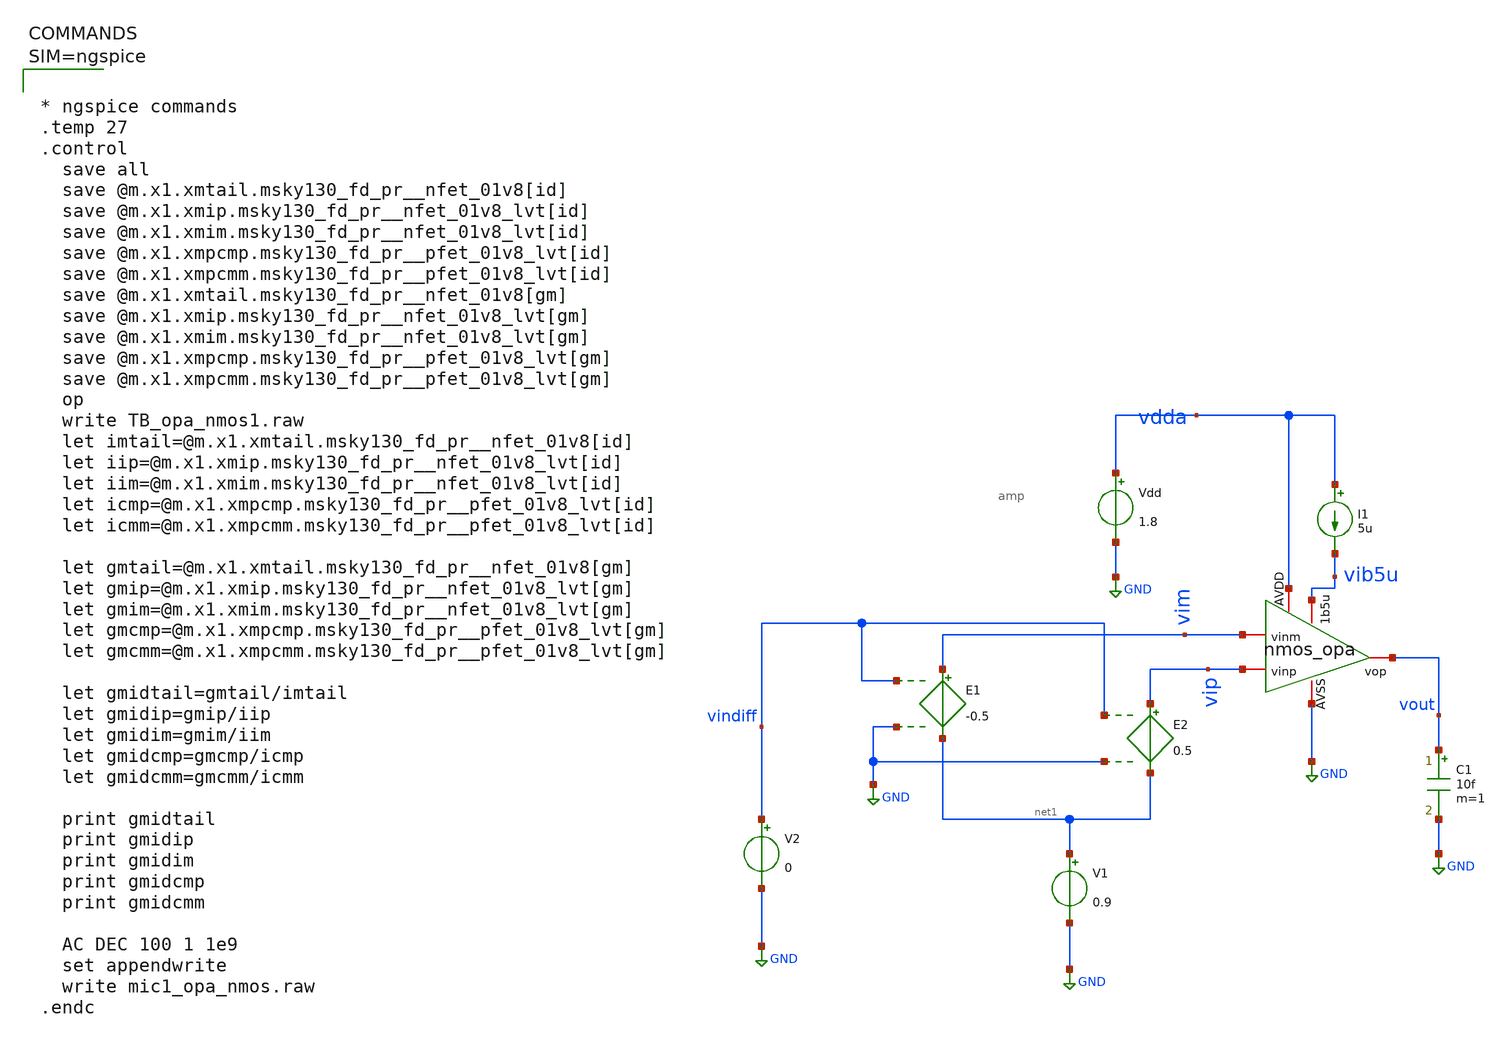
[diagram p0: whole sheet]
** sch_path: work/xschem/mic1_opa_nmos.sch
**.subckt mic1_opa_nmos
E1 vim net1 vindiff GND -0.5
E2 vip net1 vindiff GND 0.5
V1 net1 GND 0.9
V2 vindiff GND 0
Vdd vdda GND 1.8
I1 vdda vib5u 5u
C1 vout GND 10f m=1
x1 vdda vout vim vip vib5u GND amp
**** begin user architecture code

** opencircuitdesign pdks install
.lib $::SKYWATER_MODELS/sky130.lib.spice tt




* ngspice commands
.temp 27
.control
  save all
  save @m.x1.xmtail.msky130_fd_pr__nfet_01v8[id]
  save @m.x1.xmip.msky130_fd_pr__nfet_01v8_lvt[id]
  save @m.x1.xmim.msky130_fd_pr__nfet_01v8_lvt[id]
  save @m.x1.xmpcmp.msky130_fd_pr__pfet_01v8_lvt[id]
  save @m.x1.xmpcmm.msky130_fd_pr__pfet_01v8_lvt[id]
  save @m.x1.xmtail.msky130_fd_pr__nfet_01v8[gm]
  save @m.x1.xmip.msky130_fd_pr__nfet_01v8_lvt[gm]
  save @m.x1.xmim.msky130_fd_pr__nfet_01v8_lvt[gm]
  save @m.x1.xmpcmp.msky130_fd_pr__pfet_01v8_lvt[gm]
  save @m.x1.xmpcmm.msky130_fd_pr__pfet_01v8_lvt[gm]
  op
  write TB_opa_nmos1.raw
  let imtail=@m.x1.xmtail.msky130_fd_pr__nfet_01v8[id]
  let iip=@m.x1.xmip.msky130_fd_pr__nfet_01v8_lvt[id]
  let iim=@m.x1.xmim.msky130_fd_pr__nfet_01v8_lvt[id]
  let icmp=@m.x1.xmpcmp.msky130_fd_pr__pfet_01v8_lvt[id]
  let icmm=@m.x1.xmpcmm.msky130_fd_pr__pfet_01v8_lvt[id]

  let gmtail=@m.x1.xmtail.msky130_fd_pr__nfet_01v8[gm]
  let gmip=@m.x1.xmip.msky130_fd_pr__nfet_01v8_lvt[gm]
  let gmim=@m.x1.xmim.msky130_fd_pr__nfet_01v8_lvt[gm]
  let gmcmp=@m.x1.xmpcmp.msky130_fd_pr__pfet_01v8_lvt[gm]
  let gmcmm=@m.x1.xmpcmm.msky130_fd_pr__pfet_01v8_lvt[gm]

  let gmidtail=gmtail/imtail
  let gmidip=gmip/iip
  let gmidim=gmim/iim
  let gmidcmp=gmcmp/icmp
  let gmidcmm=gmcmm/icmm

  print gmidtail
  print gmidip
  print gmidim
  print gmidcmp
  print gmidcmm

  AC DEC 100 1 1e9
  set appendwrite
  write mic1_opa_nmos.raw
.endc




**** end user architecture code
**.ends

* expanding   symbol:  amp.sym # of pins=6
** sym_path: work/xschem/amp.sym
** sch_path: work/xschem/amp.sch
.subckt amp AVDD vop vinm vinp 1b5u AVSS
*.iopin vop
*.iopin vinp
*.iopin vinm
*.iopin 1b5u
*.iopin AVSS
*.iopin AVDD
XMtail net1 1b5u AVSS AVSS sky130_fd_pr__nfet_01v8 L=1 W=5 nf=1 ad='int((1 + 1)/2) * 5 / 1 * 0.29' as='int((1 + 2)/2) * 5 / 1 * 0.29'
+ pd='2*int((1 + 1)/2) * (5 / 1 + 0.29)' ps='2*int((1 + 2)/2) * (5 / 1 + 0.29)' nrd='0.29 / 5 ' nrs='0.29 / 5 '
+ sa=0 sb=0 sd=0 mult=2 m=2
XM1 1b5u 1b5u AVSS AVSS sky130_fd_pr__nfet_01v8 L=1 W=5 nf=1 ad='int((1 + 1)/2) * 5 / 1 * 0.29' as='int((1 + 2)/2) * 5 / 1 * 0.29'
+ pd='2*int((1 + 1)/2) * (5 / 1 + 0.29)' ps='2*int((1 + 2)/2) * (5 / 1 + 0.29)' nrd='0.29 / 5 ' nrs='0.29 / 5 '
+ sa=0 sb=0 sd=0 mult=1 m=1
XMpcmm vop vom AVDD AVDD sky130_fd_pr__pfet_01v8 L=2 W=5 nf=1 ad='int((nf+1)/2) * W/nf * 0.29' as='int((nf+2)/2) * W/nf * 0.29'
+ pd='2*int((nf+1)/2) * (W/nf + 0.29)' ps='2*int((nf+2)/2) * (W/nf + 0.29)' nrd='0.29 / W' nrs='0.29 / W'
+ sa=0 sb=0 sd=0 mult=2 m=2
XMpcmp vom vom AVDD AVDD sky130_fd_pr__pfet_01v8 L=2 W=5 nf=1 ad='int((nf+1)/2) * W/nf * 0.29' as='int((nf+2)/2) * W/nf * 0.29'
+ pd='2*int((nf+1)/2) * (W/nf + 0.29)' ps='2*int((nf+2)/2) * (W/nf + 0.29)' nrd='0.29 / W' nrs='0.29 / W'
+ sa=0 sb=0 sd=0 mult=2 m=2
XMim vop vinm net1 net1 sky130_fd_pr__nfet_01v8 L=2 W=5 nf=1 ad='int((1 + 1)/2) * 5 / 1 * 0.29' as='int((1 + 2)/2) * 5 / 1 * 0.29'
+ pd='2*int((1 + 1)/2) * (5 / 1 + 0.29)' ps='2*int((1 + 2)/2) * (5 / 1 + 0.29)' nrd='0.29 / 5 ' nrs='0.29 / 5 '
+ sa=0 sb=0 sd=0 mult=4 m=4
XMip vom vinp net1 net1 sky130_fd_pr__nfet_01v8 L=2 W=5 nf=1 ad='int((1 + 1)/2) * 5 / 1 * 0.29' as='int((1 + 2)/2) * 5 / 1 * 0.29'
+ pd='2*int((1 + 1)/2) * (5 / 1 + 0.29)' ps='2*int((1 + 2)/2) * (5 / 1 + 0.29)' nrd='0.29 / 5 ' nrs='0.29 / 5 '
+ sa=0 sb=0 sd=0 mult=4 m=4
**** begin user architecture code



* ngspice commands
.control
save all
write amp.raw
set appendfile
write amp.raw

.endc



**** end user architecture code
.ends

.GLOBAL GND
.end
